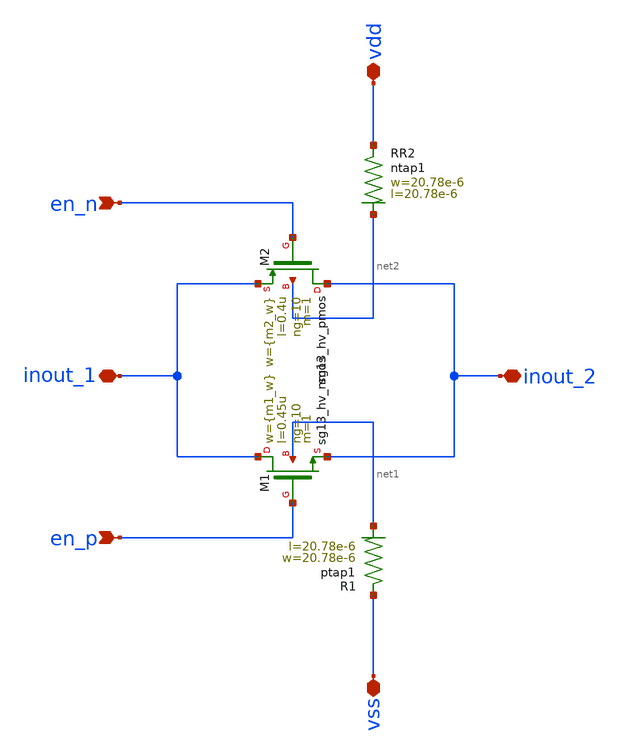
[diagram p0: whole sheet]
** sch_path: design_data/xschem/transmission_gate.sch
**.subckt transmission_gate inout_1 inout_2 en_p vdd vss en_n
*.iopin inout_1
*.iopin inout_2
*.ipin en_p
*.iopin vdd
*.iopin vss
*.ipin en_n
XM1 inout_1 en_p inout_2 net1 sg13_hv_nmos w={m1_w} l=0.45u ng=10 m=1 mm_ok=1
XM2 inout_2 en_n inout_1 net2 sg13_hv_pmos w={m2_w} l=0.4u ng=10 m=1 mm_ok=1
XR1 vss net1 ptap1 R=1.903 w=20.78e-6 l=20.78e-6
XR2 vdd net2 ntap1 R=1.903 w=20.78e-6 l=20.78e-6
**.ends
.end
